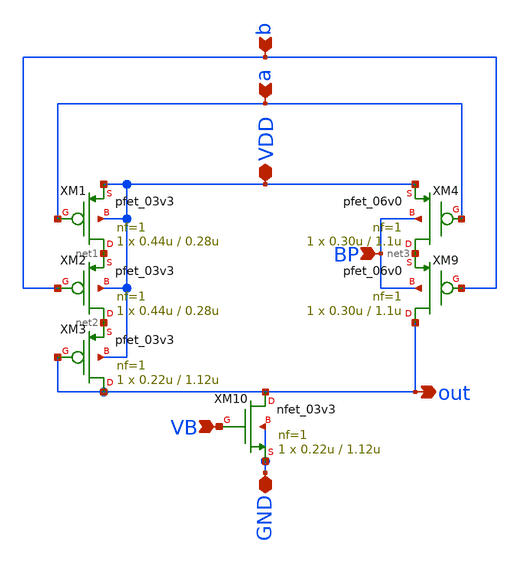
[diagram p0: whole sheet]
** sch_path: xschem_designs/NMAX_P.sch
**.subckt NMAX_P a out VDD b BP GND VB
*.ipin a
*.opin out
*.iopin VDD
*.ipin b
*.ipin BP
*.iopin GND
*.ipin VB
XM1 net1 a VDD VDD pfet_03v3 L=0.28u W=0.44u nf=1 ad='int((nf+1)/2) * W/nf * 0.18u' as='int((nf+2)/2) * W/nf * 0.18u'
+ pd='2*int((nf+1)/2) * (W/nf + 0.18u)' ps='2*int((nf+2)/2) * (W/nf + 0.18u)' nrd='0.18u / W' nrs='0.18u / W'
+ sa=0 sb=0 sd=0 m=1 par=1
XM2 net2 b net1 VDD pfet_03v3 L=0.28u W=0.44u nf=1 ad='int((nf+1)/2) * W/nf * 0.18u' as='int((nf+2)/2) * W/nf * 0.18u'
+ pd='2*int((nf+1)/2) * (W/nf + 0.18u)' ps='2*int((nf+2)/2) * (W/nf + 0.18u)' nrd='0.18u / W' nrs='0.18u / W'
+ sa=0 sb=0 sd=0 m=1 par=1
XM3 out out net2 VDD pfet_03v3 L=1.12u W=0.22u nf=1 ad='int((nf+1)/2) * W/nf * 0.18u' as='int((nf+2)/2) * W/nf * 0.18u'
+ pd='2*int((nf+1)/2) * (W/nf + 0.18u)' ps='2*int((nf+2)/2) * (W/nf + 0.18u)' nrd='0.18u / W' nrs='0.18u / W'
+ sa=0 sb=0 sd=0 m=1 par=1
XM4 net3 a VDD BP pfet_06v0 L=1.1u W=0.30u nf=1 ad='int((nf+1)/2) * W/nf * 0.18u' as='int((nf+2)/2) * W/nf * 0.18u'
+ pd='2*int((nf+1)/2) * (W/nf + 0.18u)' ps='2*int((nf+2)/2) * (W/nf + 0.18u)' nrd='0.18u / W' nrs='0.18u / W'
+ sa=0 sb=0 sd=0 m=1
XM9 out b net3 BP pfet_06v0 L=1.1u W=0.30u nf=1 ad='int((nf+1)/2) * W/nf * 0.18u' as='int((nf+2)/2) * W/nf * 0.18u'
+ pd='2*int((nf+1)/2) * (W/nf + 0.18u)' ps='2*int((nf+2)/2) * (W/nf + 0.18u)' nrd='0.18u / W' nrs='0.18u / W'
+ sa=0 sb=0 sd=0 m=1
XM10 out VB GND GND nfet_03v3 L=1.12u W=0.22u nf=1 ad='int((nf+1)/2) * W/nf * 0.18u' as='int((nf+2)/2) * W/nf * 0.18u'
+ pd='2*int((nf+1)/2) * (W/nf + 0.18u)' ps='2*int((nf+2)/2) * (W/nf + 0.18u)' nrd='0.18u / W' nrs='0.18u / W'
+ sa=0 sb=0 sd=0 m=1 par=1
**.ends
.end
